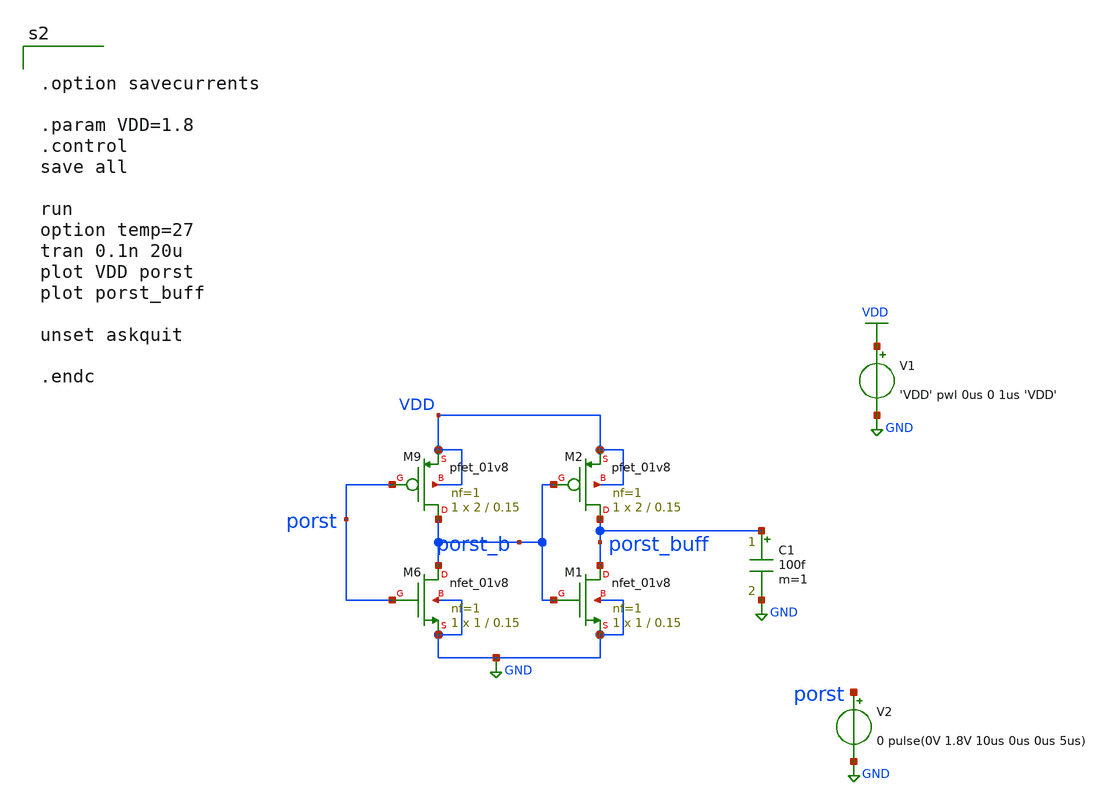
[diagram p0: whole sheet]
** sch_path: xschem/misc/testing/buffer.sch
**.subckt buffer
XM6 porst_b porst GND GND sky130_fd_pr__nfet_01v8 L=0.15 W=1 nf=1 ad='int((nf+1)/2) * W/nf * 0.29' as='int((nf+2)/2) * W/nf * 0.29'
+ pd='2*int((nf+1)/2) * (W/nf + 0.29)' ps='2*int((nf+2)/2) * (W/nf + 0.29)' nrd='0.29 / W' nrs='0.29 / W'
+ sa=0 sb=0 sd=0 mult=1 m=1
XM9 porst_b porst VDD VDD sky130_fd_pr__pfet_01v8 L=0.15 W=2 nf=1 ad='int((nf+1)/2) * W/nf * 0.29' as='int((nf+2)/2) * W/nf * 0.29'
+ pd='2*int((nf+1)/2) * (W/nf + 0.29)' ps='2*int((nf+2)/2) * (W/nf + 0.29)' nrd='0.29 / W' nrs='0.29 / W'
+ sa=0 sb=0 sd=0 mult=1 m=1
XM1 porst_buff porst_b GND GND sky130_fd_pr__nfet_01v8 L=0.15 W=1 nf=1 ad='int((nf+1)/2) * W/nf * 0.29'
+ as='int((nf+2)/2) * W/nf * 0.29' pd='2*int((nf+1)/2) * (W/nf + 0.29)' ps='2*int((nf+2)/2) * (W/nf + 0.29)'
+ nrd='0.29 / W' nrs='0.29 / W' sa=0 sb=0 sd=0 mult=1 m=1
XM2 porst_buff porst_b VDD VDD sky130_fd_pr__pfet_01v8 L=0.15 W=2 nf=1 ad='int((nf+1)/2) * W/nf * 0.29'
+ as='int((nf+2)/2) * W/nf * 0.29' pd='2*int((nf+1)/2) * (W/nf + 0.29)' ps='2*int((nf+2)/2) * (W/nf + 0.29)'
+ nrd='0.29 / W' nrs='0.29 / W' sa=0 sb=0 sd=0 mult=1 m=1
V1 VDD GND 'VDD' pwl 0us 0 1us 'VDD'
V2 porst GND 0 pulse(0V 1.8V 10us 0us 0us 5us)
C1 porst_buff GND 100f m=1
**** begin user architecture code

** opencircuitdesign pdks install
.lib $::SKYWATER_MODELS/sky130.lib.spice tt




.option savecurrents

.param VDD=1.8
.control
save all

run
option temp=27
tran 0.1n 20u
plot VDD porst
plot porst_buff

unset askquit

.endc


**** end user architecture code
**.ends
.GLOBAL VDD
.GLOBAL GND
.end
